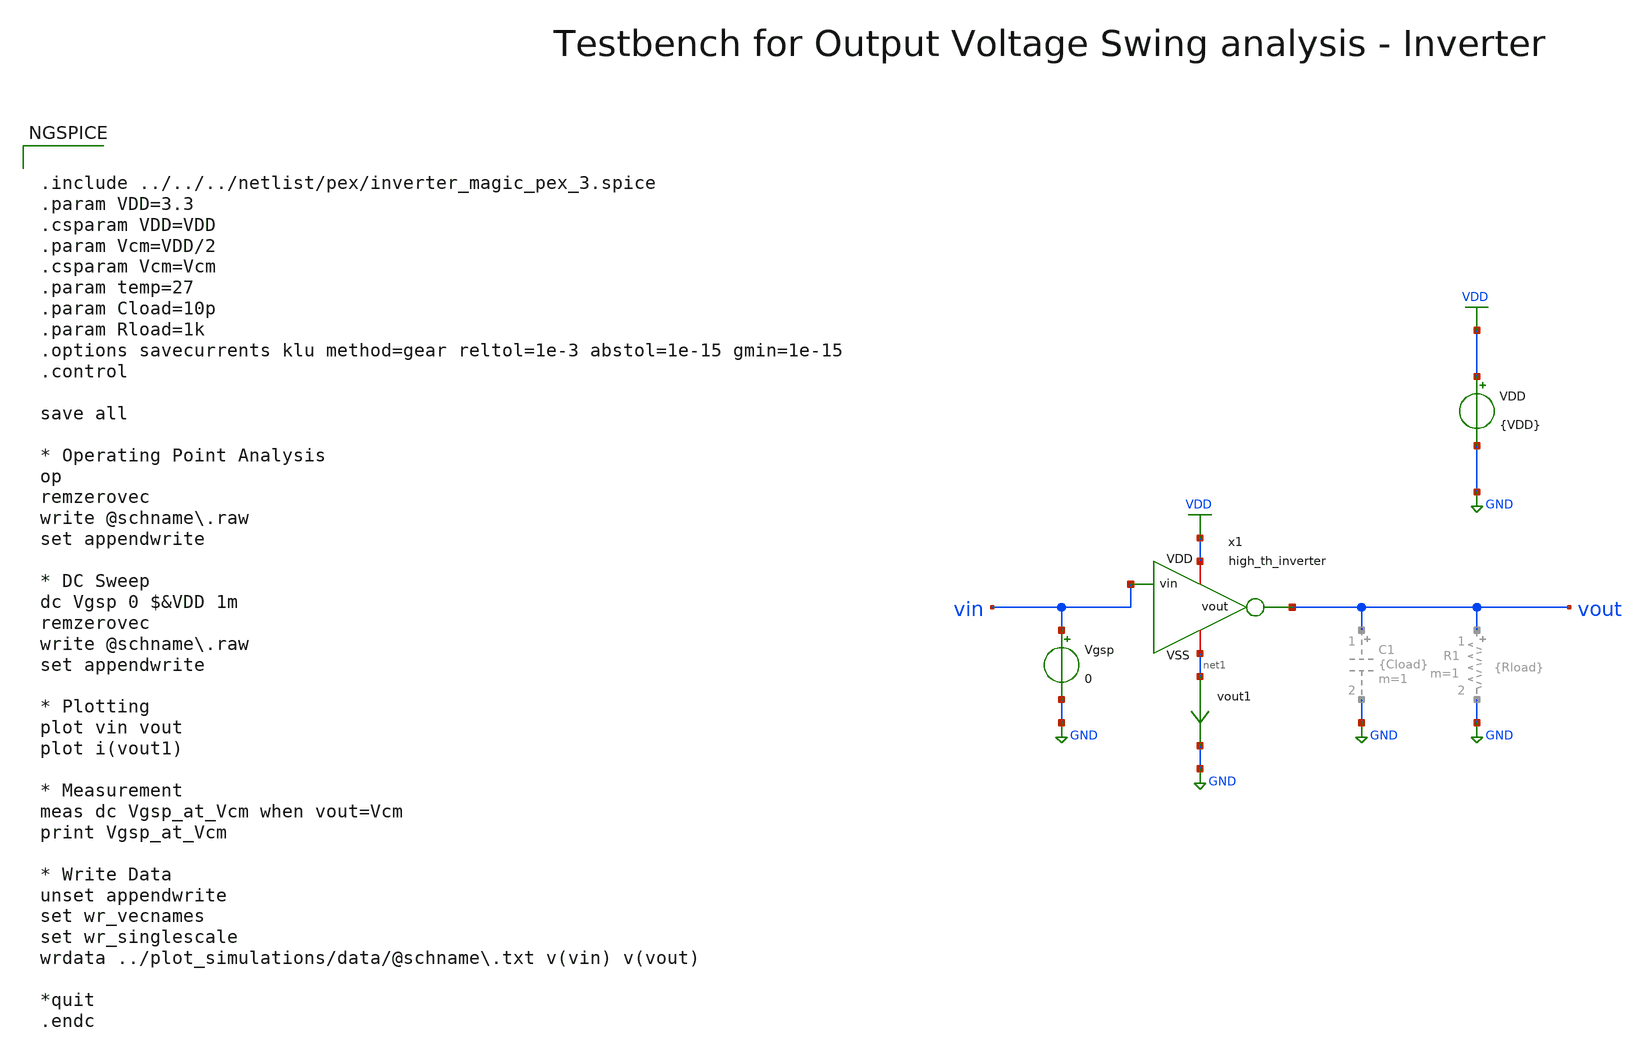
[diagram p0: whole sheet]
** sch_path: macros/heichips26_vcr/macros/switched_capacitor/testbenches/xschem/hth_inv_dc_vout.sch
**.subckt hth_inv_dc_vout
VDD VDD GND {VDD}
Vgsp vin GND 0
x1 VDD vin vout net1 high_th_inverter
vout1 net1 GND 0
.save i(vout1)
**** begin user architecture code


.include ../../../netlist/pex/inverter_magic_pex_3.spice
.param VDD=3.3
.csparam VDD=VDD
.param Vcm=VDD/2
.csparam Vcm=Vcm
.param temp=27
.param Cload=10p
.param Rload=1k
.options savecurrents klu method=gear reltol=1e-3 abstol=1e-15 gmin=1e-15
.control

save all

* Operating Point Analysis
op
remzerovec
write @schname\.raw
set appendwrite

* DC Sweep
dc Vgsp 0 $&VDD 1m
remzerovec
write @schname\.raw
set appendwrite

* Plotting
plot vin vout
plot i(vout1)

* Measurement
meas dc Vgsp_at_Vcm when vout=Vcm
print Vgsp_at_Vcm

* Write Data
unset appendwrite
set wr_vecnames
set wr_singlescale
wrdata ../plot_simulations/data/@schname\.txt v(vin) v(vout)

*quit
.endc



.lib cornerMOSlv.lib mos_tt
.lib cornerMOShv.lib mos_tt
.lib cornerRES.lib res_typ
.lib cornerDIO.lib dio_tt

**** end user architecture code
**.ends

* expanding   symbol:  high_th_inverter.sym # of pins=4
** sym_path: macros/heichips26_vcr/macros/switched_capacitor/schematic/xschem/high_th_inverter.sym
** sch_path: macros/heichips26_vcr/macros/switched_capacitor/schematic/xschem/high_th_inverter.sch
.subckt high_th_inverter VDD vin vout VSS
*.ipin vin
*.iopin VDD
*.iopin VSS
*.opin vout
XMdummy1 VSS VSS VSS VSS sg13_hv_nmos w=0.6u l=1.0u ng=2 m=1 mm_ok=1
XMdummy2 VDD VDD VDD VDD sg13_hv_pmos w=12.0u l=1.0u ng=2 m=1 mm_ok=1
XM1 vout vin VSS VSS sg13_hv_nmos w=6.0u l=1.0u ng=20 m=1 mm_ok=1
XM2 vout vin VDD VDD sg13_hv_pmos w=120.0u l=1.0u ng=20 m=1 mm_ok=1
.ends

.GLOBAL GND
.GLOBAL VDD
.end
